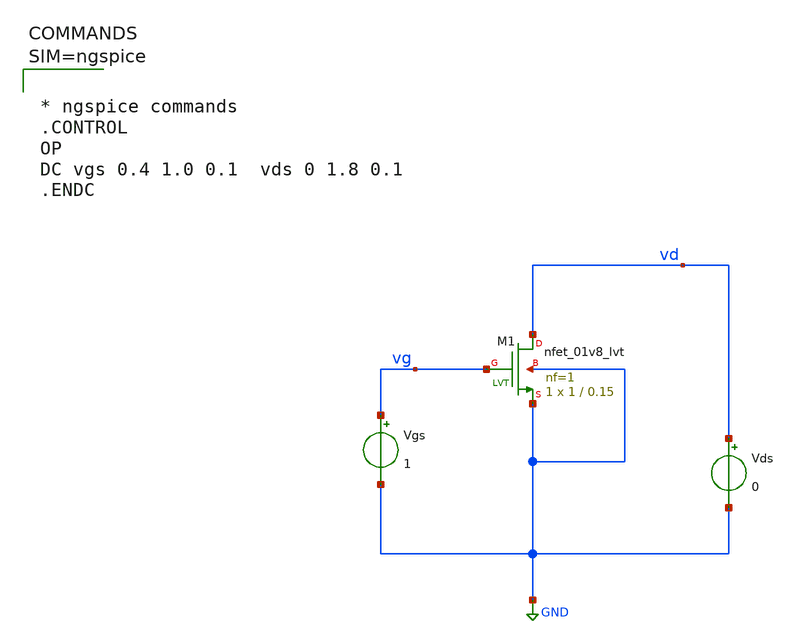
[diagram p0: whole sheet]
** sch_path: xschem/IDvdsNMOS.sch
**.subckt IDvdsNMOS
XM1 vd vg GND GND sky130_fd_pr__nfet_01v8_lvt L=0.15 W=1 nf=1 ad='int((1 + 1)/2) * 1 / 1 * 0.29' as='int((1 + 2)/2) * 1 / 1 * 0.29'
+ pd='2*int((1 + 1)/2) * (1 / 1 + 0.29)' ps='2*int((1 + 2)/2) * (1 / 1 + 0.29)' nrd='0.29 / 1 ' nrs='0.29 / 1 '
+ sa=0 sb=0 sd=0 mult=1 m=1
Vgs vg GND 1
Vds vd GND 0
**** begin user architecture code

** opencircuitdesign pdks install
.lib $::SKYWATER_MODELS/sky130.lib.spice tt




* ngspice commands
.CONTROL
OP
DC vgs 0.4 1.0 0.1  vds 0 1.8 0.1
.ENDC



**** end user architecture code
**.ends
.GLOBAL GND
.end
